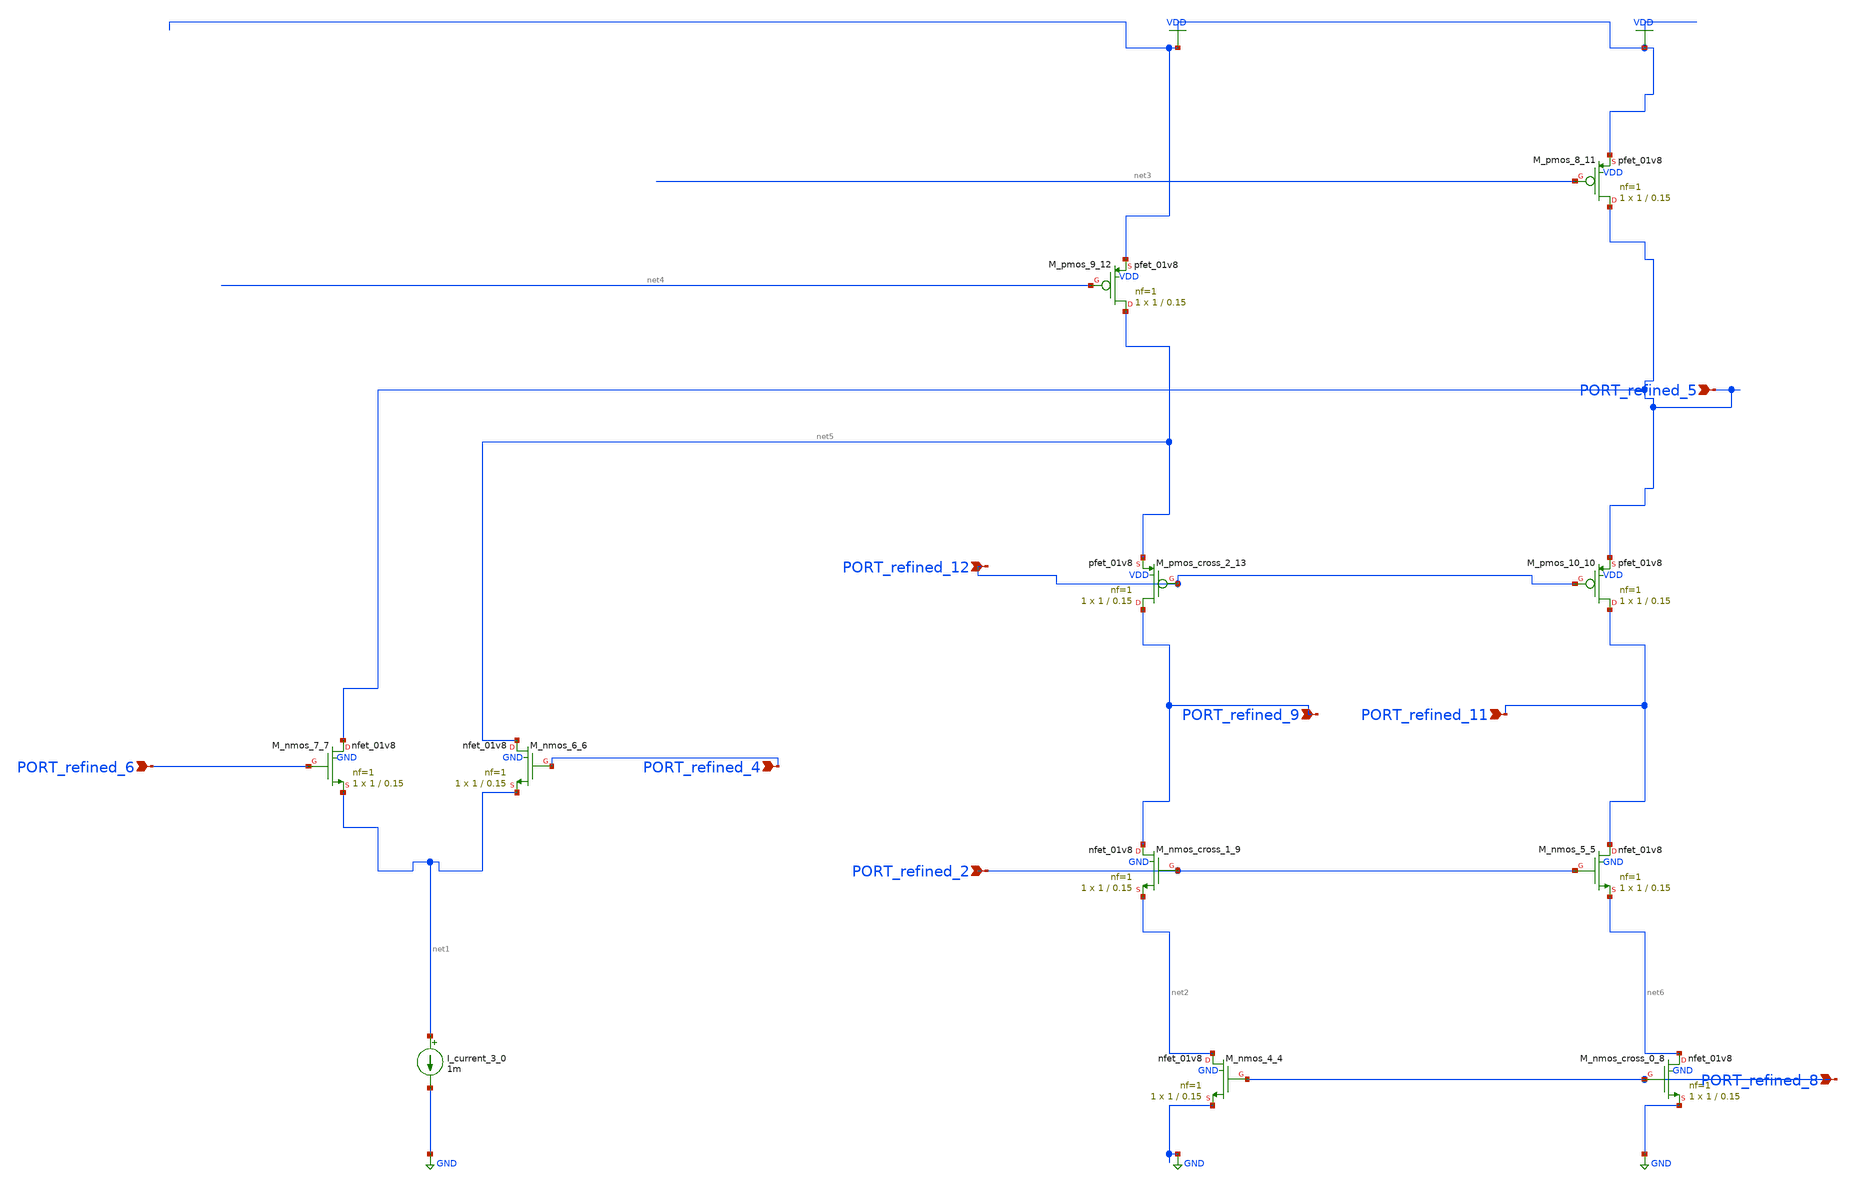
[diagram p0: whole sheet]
** sch_path: schematics/AMSNet/744.sch
**.subckt 744 PORT_refined_4 PORT_refined_9 PORT_refined_2 PORT_refined_12 PORT_refined_11
*+ PORT_refined_8 PORT_refined_6 PORT_refined_5
*.ipin PORT_refined_4
*.ipin PORT_refined_9
*.ipin PORT_refined_2
*.ipin PORT_refined_12
*.ipin PORT_refined_11
*.ipin PORT_refined_8
*.ipin PORT_refined_6
*.ipin PORT_refined_5
I_current_3_0 net1 GND 1m
XM_nmos_4_4 net2 PORT_refined_8 GND GND sky130_fd_pr__nfet_01v8 L=0.15 W=1 nf=1 ad='int((1 + 1)/2) * 1 / 1 * 0.29'
+ as='int((1 + 2)/2) * 1 / 1 * 0.29' pd='2*int((1 + 1)/2) * (1 / 1 + 0.29)' ps='2*int((1 + 2)/2) * (1 / 1 + 0.29)'
+ nrd='0.29 / 1 ' nrs='0.29 / 1 ' sa=0 sb=0 sd=0 mult=1 m=1
XM_nmos_5_5 PORT_refined_11 PORT_refined_2 net6 GND sky130_fd_pr__nfet_01v8 L=0.15 W=1 nf=1 ad='int((1 + 1)/2) * 1 / 1 * 0.29'
+ as='int((1 + 2)/2) * 1 / 1 * 0.29' pd='2*int((1 + 1)/2) * (1 / 1 + 0.29)' ps='2*int((1 + 2)/2) * (1 / 1 + 0.29)'
+ nrd='0.29 / 1 ' nrs='0.29 / 1 ' sa=0 sb=0 sd=0 mult=1 m=1
XM_nmos_6_6 net5 PORT_refined_4 net1 GND sky130_fd_pr__nfet_01v8 L=0.15 W=1 nf=1 ad='int((1 + 1)/2) * 1 / 1 * 0.29'
+ as='int((1 + 2)/2) * 1 / 1 * 0.29' pd='2*int((1 + 1)/2) * (1 / 1 + 0.29)' ps='2*int((1 + 2)/2) * (1 / 1 + 0.29)'
+ nrd='0.29 / 1 ' nrs='0.29 / 1 ' sa=0 sb=0 sd=0 mult=1 m=1
XM_nmos_7_7 PORT_refined_5 PORT_refined_6 net1 GND sky130_fd_pr__nfet_01v8 L=0.15 W=1 nf=1 ad='int((1 + 1)/2) * 1 / 1 * 0.29'
+ as='int((1 + 2)/2) * 1 / 1 * 0.29' pd='2*int((1 + 1)/2) * (1 / 1 + 0.29)' ps='2*int((1 + 2)/2) * (1 / 1 + 0.29)'
+ nrd='0.29 / 1 ' nrs='0.29 / 1 ' sa=0 sb=0 sd=0 mult=1 m=1
XM_nmos_cross_0_8 net6 PORT_refined_8 GND GND sky130_fd_pr__nfet_01v8 L=0.15 W=1 nf=1 ad='int((1 + 1)/2) * 1 / 1 * 0.29'
+ as='int((1 + 2)/2) * 1 / 1 * 0.29' pd='2*int((1 + 1)/2) * (1 / 1 + 0.29)' ps='2*int((1 + 2)/2) * (1 / 1 + 0.29)'
+ nrd='0.29 / 1 ' nrs='0.29 / 1 ' sa=0 sb=0 sd=0 mult=1 m=1
XM_nmos_cross_1_9 PORT_refined_9 PORT_refined_2 net2 GND sky130_fd_pr__nfet_01v8 L=0.15 W=1 nf=1 ad='int((1 + 1)/2) * 1 / 1 * 0.29'
+ as='int((1 + 2)/2) * 1 / 1 * 0.29' pd='2*int((1 + 1)/2) * (1 / 1 + 0.29)' ps='2*int((1 + 2)/2) * (1 / 1 + 0.29)'
+ nrd='0.29 / 1 ' nrs='0.29 / 1 ' sa=0 sb=0 sd=0 mult=1 m=1
XM_pmos_10_10 PORT_refined_11 PORT_refined_12 PORT_refined_5 VDD sky130_fd_pr__pfet_01v8 L=0.15 W=1 nf=1
+ ad='int((1 + 1)/2) * 1 / 1 * 0.29' as='int((1 + 2)/2) * 1 / 1 * 0.29' pd='2*int((1 + 1)/2) * (1 / 1 + 0.29)'
+ ps='2*int((1 + 2)/2) * (1 / 1 + 0.29)' nrd='0.29 / 1 ' nrs='0.29 / 1 ' sa=0 sb=0 sd=0 mult=1 m=1
XM_pmos_8_11 PORT_refined_5 net3 VDD VDD sky130_fd_pr__pfet_01v8 L=0.15 W=1 nf=1 ad='int((1 + 1)/2) * 1 / 1 * 0.29'
+ as='int((1 + 2)/2) * 1 / 1 * 0.29' pd='2*int((1 + 1)/2) * (1 / 1 + 0.29)' ps='2*int((1 + 2)/2) * (1 / 1 + 0.29)'
+ nrd='0.29 / 1 ' nrs='0.29 / 1 ' sa=0 sb=0 sd=0 mult=1 m=1
XM_pmos_9_12 net5 net4 VDD VDD sky130_fd_pr__pfet_01v8 L=0.15 W=1 nf=1 ad='int((1 + 1)/2) * 1 / 1 * 0.29'
+ as='int((1 + 2)/2) * 1 / 1 * 0.29' pd='2*int((1 + 1)/2) * (1 / 1 + 0.29)' ps='2*int((1 + 2)/2) * (1 / 1 + 0.29)'
+ nrd='0.29 / 1 ' nrs='0.29 / 1 ' sa=0 sb=0 sd=0 mult=1 m=1
XM_pmos_cross_2_13 PORT_refined_9 PORT_refined_12 net5 VDD sky130_fd_pr__pfet_01v8 L=0.15 W=1 nf=1 ad='int((1 + 1)/2) * 1 / 1 * 0.29'
+ as='int((1 + 2)/2) * 1 / 1 * 0.29' pd='2*int((1 + 1)/2) * (1 / 1 + 0.29)' ps='2*int((1 + 2)/2) * (1 / 1 + 0.29)'
+ nrd='0.29 / 1 ' nrs='0.29 / 1 ' sa=0 sb=0 sd=0 mult=1 m=1
**.ends
.GLOBAL GND
.GLOBAL VDD
.end
